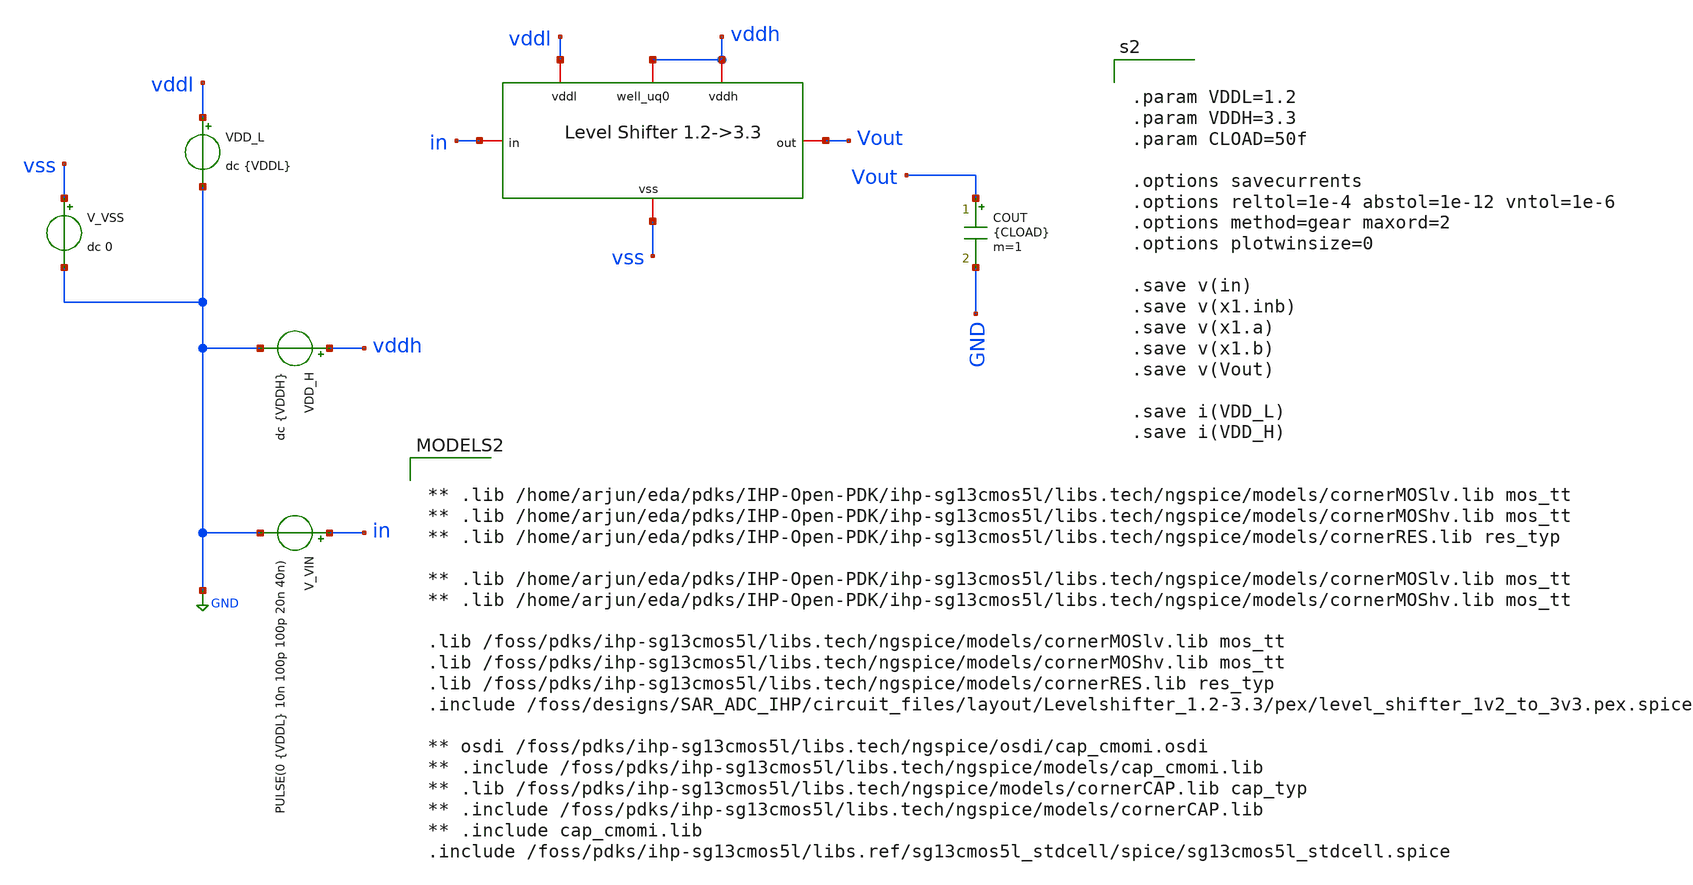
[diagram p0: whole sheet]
** sch_path: circuit_files/tb/LS_l2h_tb_pex.sch
**.subckt LS_l2h_tb_pex
V_VIN in GND PULSE(0 {VDDL} 10n 100p 100p 20n 40n)
VDD_L vddl GND dc {VDDL}
VDD_H vddh GND dc {VDDH}
V_VSS vss GND dc 0
COUT Vout GND {CLOAD} m=1
x3 vss vddl in Vout vddh vddh level_shifter_1v2_to_3v3_pex
**** begin user architecture code

** .lib /home/arjun/eda/pdks/IHP-Open-PDK/ihp-sg13cmos5l/libs.tech/ngspice/models/cornerMOSlv.lib
*+ mos_tt
** .lib /home/arjun/eda/pdks/IHP-Open-PDK/ihp-sg13cmos5l/libs.tech/ngspice/models/cornerMOShv.lib
*+ mos_tt
** .lib /home/arjun/eda/pdks/IHP-Open-PDK/ihp-sg13cmos5l/libs.tech/ngspice/models/cornerRES.lib
*+ res_typ

** .lib /home/arjun/eda/pdks/IHP-Open-PDK/ihp-sg13cmos5l/libs.tech/ngspice/models/cornerMOSlv.lib
*+ mos_tt
** .lib /home/arjun/eda/pdks/IHP-Open-PDK/ihp-sg13cmos5l/libs.tech/ngspice/models/cornerMOShv.lib
*+ mos_tt

.lib /foss/pdks/ihp-sg13cmos5l/libs.tech/ngspice/models/cornerMOSlv.lib mos_tt
.lib /foss/pdks/ihp-sg13cmos5l/libs.tech/ngspice/models/cornerMOShv.lib mos_tt
.lib /foss/pdks/ihp-sg13cmos5l/libs.tech/ngspice/models/cornerRES.lib res_typ
.include /foss/designs/SAR_ADC_IHP/circuit_files/layout/Levelshifter_1.2-3.3/pex/level_shifter_1v2_to_3v3.pex.spice

** osdi /foss/pdks/ihp-sg13cmos5l/libs.tech/ngspice/osdi/cap_cmomi.osdi
** .include /foss/pdks/ihp-sg13cmos5l/libs.tech/ngspice/models/cap_cmomi.lib
** .lib /foss/pdks/ihp-sg13cmos5l/libs.tech/ngspice/models/cornerCAP.lib cap_typ
** .include /foss/pdks/ihp-sg13cmos5l/libs.tech/ngspice/models/cornerCAP.lib
** .include cap_cmomi.lib
.include /foss/pdks/ihp-sg13cmos5l/libs.ref/sg13cmos5l_stdcell/spice/sg13cmos5l_stdcell.spice




.param VDDL=1.2
.param VDDH=3.3
.param CLOAD=50f

.options savecurrents
.options reltol=1e-4 abstol=1e-12 vntol=1e-6
.options method=gear maxord=2
.options plotwinsize=0

.save v(in)
.save v(x1.inb)
.save v(x1.a)
.save v(x1.b)
.save v(Vout)

.save i(VDD_L)
.save i(VDD_H)




.control

set noaskquit
set filetype=binary
set wr_singlescale
set wr_vecnames

shell rm -f level_shifter_pex_results.txt
shell rm -f level_shifter_pex.raw

echo ============================================================ > level_shifter_pex_results.txt
echo IHP SG13CMOS5L LEVEL SHIFTER PEX TRANSIENT TEST >> level_shifter_pex_results.txt
echo ============================================================ >> level_shifter_pex_results.txt
echo VDDL = 1.2 V >> level_shifter_pex_results.txt
echo VDDH = 3.3 V >> level_shifter_pex_results.txt
echo CLOAD = 50 fF >> level_shifter_pex_results.txt
echo Output limits: LOW < 0.33 V, HIGH > 2.97 V >> level_shifter_pex_results.txt

* Use the nominal values already defined in the testbench
alterparam VDDL=1.2
alterparam VDDH=3.3
alterparam CLOAD=50f

reset

* Input source is expected to be:
* PULSE(0 {VDDL} 10n 100p 100p 20n 40n)
*
* Input:
*   LOW  approximately 0–10 ns
*   HIGH approximately 10–30 ns
*   LOW  approximately 30–50 ns
*   HIGH approximately 50–70 ns
*
* Run long enough to capture two complete transitions.
tran 10p 90n

* Save the PEX transient waveform
write level_shifter_pex.raw v(in) v(Vout) v(vddl) v(vddh) v(vss) i(VDD_L) i(VDD_H)

* ============================================================
* STATIC LOGIC LEVELS
* ============================================================

* Input HIGH
meas tran in_high FIND v(in) AT=25n
meas tran out_high FIND v(Vout) AT=25n

* Input LOW
meas tran in_low FIND v(in) AT=45n
meas tran out_low FIND v(Vout) AT=45n

let high_limit = 0.9*VDDH
let low_limit  = 0.1*VDDH

let err_high = out_high - VDDH
let err_low  = out_low

* ============================================================
* PROPAGATION DELAY
* ============================================================

* Input threshold = VDDL/2 = 0.6 V
* Output threshold = VDDH/2 = 1.65 V
*
* Use the second complete transition.
meas tran tplh TRIG v(in) VAL=0.6 RISE=2 TARG v(Vout) VAL=1.65 RISE=2
meas tran tphl TRIG v(in) VAL=0.6 FALL=2 TARG v(Vout) VAL=1.65 FALL=2

* ============================================================
* OUTPUT RISE/FALL TIME
* ============================================================

meas tran tr_out TRIG v(Vout) VAL=0.33 RISE=2 TARG v(Vout) VAL=2.97 RISE=2
meas tran tf_out TRIG v(Vout) VAL=2.97 FALL=2 TARG v(Vout) VAL=0.33 FALL=2

* ============================================================
* SUPPLY CURRENT AND POWER
* ============================================================

meas tran iddl_avg AVG i(VDD_L) FROM=10n TO=90n
meas tran iddh_avg AVG i(VDD_H) FROM=10n TO=90n

let p_vddl = abs(VDDL*iddl_avg)
let p_vddh = abs(VDDH*iddh_avg)
let p_total = p_vddl + p_vddh

* ============================================================
* PASS CONDITIONS
*
* Output HIGH must be > 90% of VDDH
* Output LOW must be < 10% of VDDH
* ============================================================

let pass_high = 0
if out_high > high_limit
  let pass_high = 1
end

let pass_low = 0
if out_low < low_limit
  let pass_low = 1
end

let functional_pass = 0
if pass_high = 1
  if pass_low = 1
    let functional_pass = 1
  end
end

* ============================================================
* WRITE RESULTS
* ============================================================

echo ------------------------------------------------------------ >> level_shifter_pex_results.txt
echo STATIC LEVELS >> level_shifter_pex_results.txt
echo ------------------------------------------------------------ >> level_shifter_pex_results.txt
echo Input_HIGH = $&in_high V >> level_shifter_pex_results.txt
echo Output_HIGH = $&out_high V >> level_shifter_pex_results.txt
echo High_error = $&err_high V >> level_shifter_pex_results.txt
echo Input_LOW = $&in_low V >> level_shifter_pex_results.txt
echo Output_LOW = $&out_low V >> level_shifter_pex_results.txt
echo Low_error = $&err_low V >> level_shifter_pex_results.txt

echo ------------------------------------------------------------ >> level_shifter_pex_results.txt
echo TIMING >> level_shifter_pex_results.txt
echo ------------------------------------------------------------ >> level_shifter_pex_results.txt
echo TPLH = $&tplh s >> level_shifter_pex_results.txt
echo TPHL = $&tphl s >> level_shifter_pex_results.txt
echo Output_rise_10_to_90 = $&tr_out s >> level_shifter_pex_results.txt
echo Output_fall_90_to_10 = $&tf_out s >> level_shifter_pex_results.txt

echo ------------------------------------------------------------ >> level_shifter_pex_results.txt
echo POWER >> level_shifter_pex_results.txt
echo ------------------------------------------------------------ >> level_shifter_pex_results.txt
echo VDDL_power = $&p_vddl W >> level_shifter_pex_results.txt
echo VDDH_power = $&p_vddh W >> level_shifter_pex_results.txt
echo Total_average_power = $&p_total W >> level_shifter_pex_results.txt

echo ------------------------------------------------------------ >> level_shifter_pex_results.txt
echo PASS RESULT >> level_shifter_pex_results.txt
echo ------------------------------------------------------------ >> level_shifter_pex_results.txt
echo Pass_HIGH = $&pass_high >> level_shifter_pex_results.txt
echo Pass_LOW = $&pass_low >> level_shifter_pex_results.txt
echo FUNCTIONAL_PASS = $&functional_pass >> level_shifter_pex_results.txt

* Optional ASCII waveform file
wrdata level_shifter_pex_waveforms.txt v(in) v(Vout) v(vddl) v(vddh) v(vss)

* Display waveforms if running interactively
plot v(in) v(Vout)
plot v(vddl) v(vddh) v(Vout)

.endc



**** end user architecture code
**.ends
.GLOBAL GND
.end
